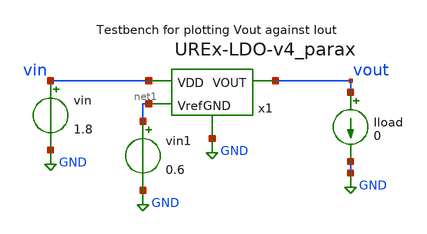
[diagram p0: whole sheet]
** sch_path: xschem/testbenches/postlayout/VoutvsIout-v4-postlayout.sch
**.subckt VoutvsIout-v4-postlayout
vin vin GND 1.8
x1 vin vout GND net1 UREx-LDO-v4_parax
vin1 net1 GND 0.6
Iload vout GND 0
**** begin user architecture code



.lib /usr/local/share/pdk/sky130A/libs.tech/ngspice/sky130.lib.spice tt
*.tran 1m 1n
.dc Iload 1n 1m 0.01um

.control
run
plot v(vout)
.endc


**** end user architecture code
**.ends

* expanding   symbol:  UREx-LDO-v4_parax.sym # of pins=4
** sym_path: xschem/UREx-LDO-v4.sym
.include [file normalize UREx-LDO-v4_parax.spice]
.GLOBAL GND
.end
